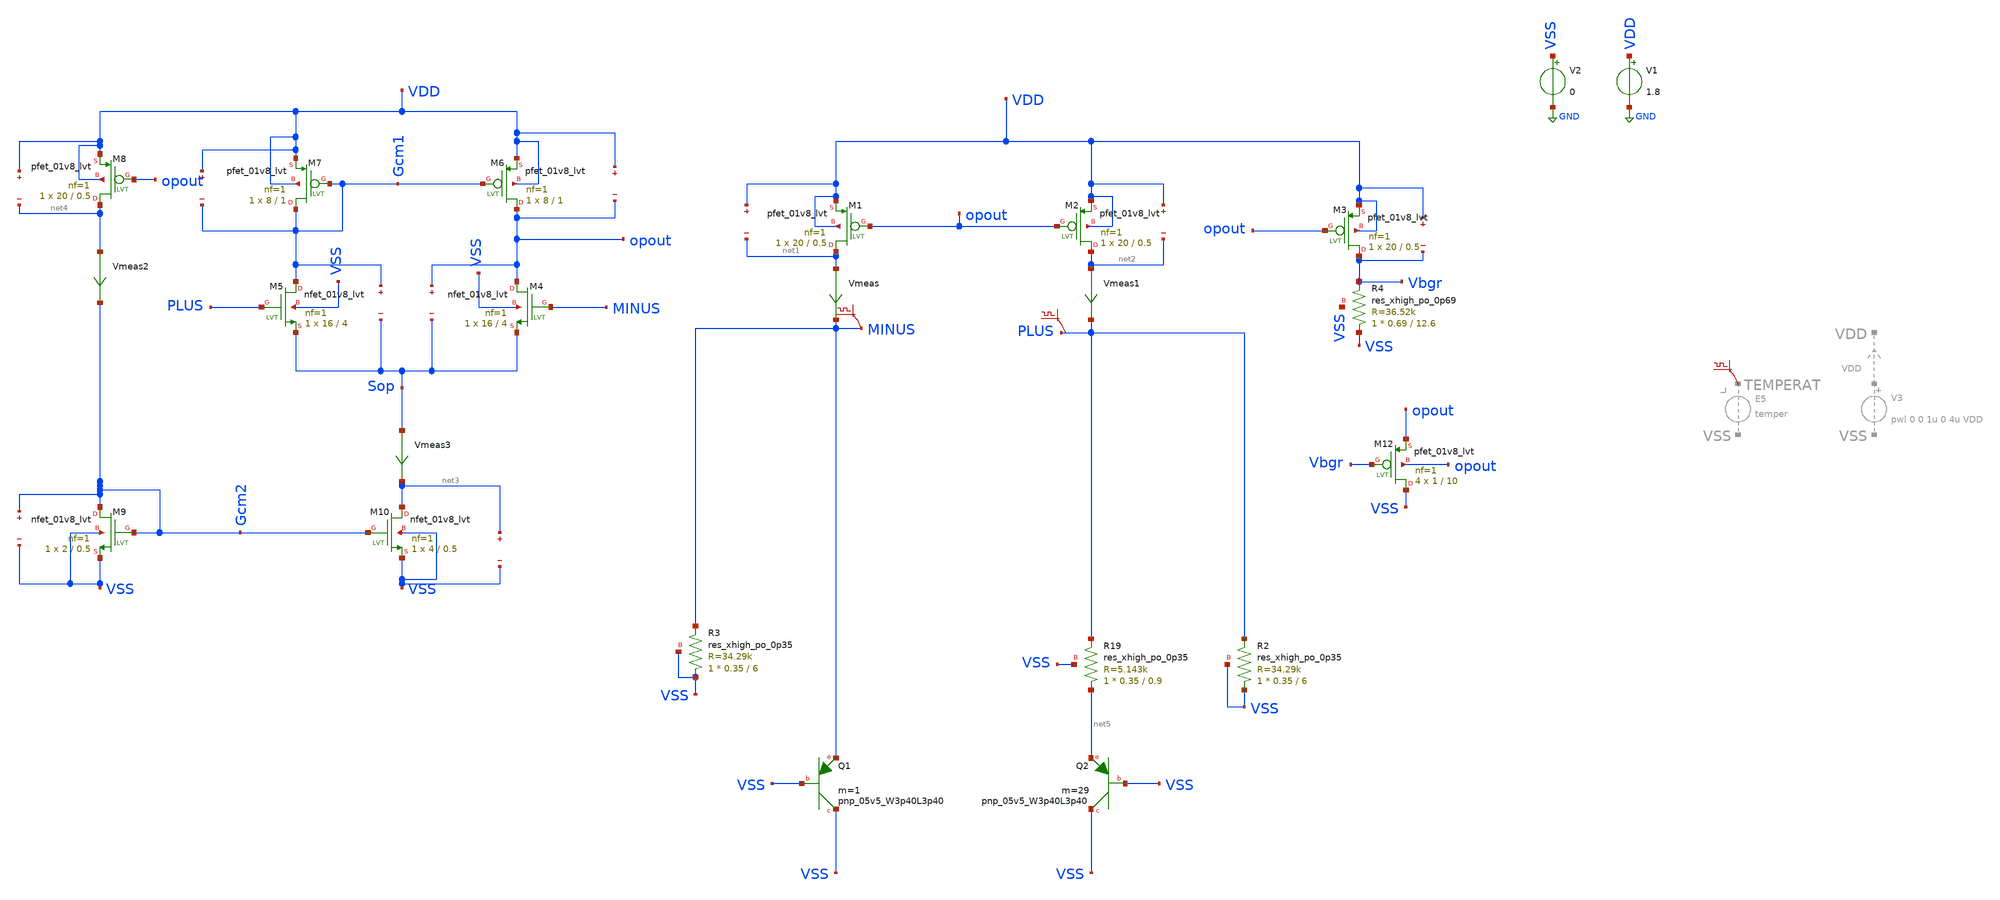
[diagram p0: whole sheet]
** sch_path: xschem/BGRwOpampRes.sch
**.subckt BGRwOpampRes
XQ1 VSS VSS MINUS sky130_fd_pr__pnp_05v5_W3p40L3p40 m=1
XQ2 VSS VSS net5 sky130_fd_pr__pnp_05v5_W3p40L3p40 m=29
XM1 net1 opout VDD VDD sky130_fd_pr__pfet_01v8_lvt L=0.5 W=20 nf=1 ad='int((nf+1)/2) * W/nf * 0.29' as='int((nf+2)/2) * W/nf * 0.29'
+ pd='2*int((nf+1)/2) * (W/nf + 0.29)' ps='2*int((nf+2)/2) * (W/nf + 0.29)' nrd='0.29 / W' nrs='0.29 / W'
+ sa=0 sb=0 sd=0 mult=1 m=1
XM2 net2 opout VDD VDD sky130_fd_pr__pfet_01v8_lvt L=0.5 W=20 nf=1 ad='int((nf+1)/2) * W/nf * 0.29' as='int((nf+2)/2) * W/nf * 0.29'
+ pd='2*int((nf+1)/2) * (W/nf + 0.29)' ps='2*int((nf+2)/2) * (W/nf + 0.29)' nrd='0.29 / W' nrs='0.29 / W'
+ sa=0 sb=0 sd=0 mult=1 m=1
XM3 Vbgr opout VDD VDD sky130_fd_pr__pfet_01v8_lvt L=0.5 W=20 nf=1 ad='int((nf+1)/2) * W/nf * 0.29' as='int((nf+2)/2) * W/nf * 0.29'
+ pd='2*int((nf+1)/2) * (W/nf + 0.29)' ps='2*int((nf+2)/2) * (W/nf + 0.29)' nrd='0.29 / W' nrs='0.29 / W'
+ sa=0 sb=0 sd=0 mult=1 m=1
V1 VDD GND 1.8
V2 VSS GND 0
Vmeas net1 MINUS 0
.save i(vmeas)
Vmeas1 net2 PLUS 0
.save i(vmeas1)
.save v(vdd)
.save v(net1)
.save v(vdd)
.save v(net2)
.save v(vdd)
.save v(vbgr)
XM4 opout MINUS Sop VSS sky130_fd_pr__nfet_01v8_lvt L=4 W=16 nf=1 ad='int((nf+1)/2) * W/nf * 0.29' as='int((nf+2)/2) * W/nf * 0.29'
+ pd='2*int((nf+1)/2) * (W/nf + 0.29)' ps='2*int((nf+2)/2) * (W/nf + 0.29)' nrd='0.29 / W' nrs='0.29 / W'
+ sa=0 sb=0 sd=0 mult=1 m=1
XM5 Gcm1 PLUS Sop VSS sky130_fd_pr__nfet_01v8_lvt L=4 W=16 nf=1 ad='int((nf+1)/2) * W/nf * 0.29' as='int((nf+2)/2) * W/nf * 0.29'
+ pd='2*int((nf+1)/2) * (W/nf + 0.29)' ps='2*int((nf+2)/2) * (W/nf + 0.29)' nrd='0.29 / W' nrs='0.29 / W'
+ sa=0 sb=0 sd=0 mult=1 m=1
XM6 opout Gcm1 VDD VDD sky130_fd_pr__pfet_01v8_lvt L=1 W=8 nf=1 ad='int((nf+1)/2) * W/nf * 0.29' as='int((nf+2)/2) * W/nf * 0.29'
+ pd='2*int((nf+1)/2) * (W/nf + 0.29)' ps='2*int((nf+2)/2) * (W/nf + 0.29)' nrd='0.29 / W' nrs='0.29 / W'
+ sa=0 sb=0 sd=0 mult=1 m=1
.save v(opout)
.save v(sop)
.save v(gcm1)
.save v(sop)
XM10 net3 Gcm2 VSS VSS sky130_fd_pr__nfet_01v8_lvt L=0.5 W=4 nf=1 ad='int((nf+1)/2) * W/nf * 0.29' as='int((nf+2)/2) * W/nf * 0.29'
+ pd='2*int((nf+1)/2) * (W/nf + 0.29)' ps='2*int((nf+2)/2) * (W/nf + 0.29)' nrd='0.29 / W' nrs='0.29 / W'
+ sa=0 sb=0 sd=0 mult=1 m=1
XM9 Gcm2 Gcm2 VSS VSS sky130_fd_pr__nfet_01v8_lvt L=0.5 W=2 nf=1 ad='int((nf+1)/2) * W/nf * 0.29' as='int((nf+2)/2) * W/nf * 0.29'
+ pd='2*int((nf+1)/2) * (W/nf + 0.29)' ps='2*int((nf+2)/2) * (W/nf + 0.29)' nrd='0.29 / W' nrs='0.29 / W'
+ sa=0 sb=0 sd=0 mult=1 m=1
XM7 Gcm1 Gcm1 VDD VDD sky130_fd_pr__pfet_01v8_lvt L=1 W=8 nf=1 ad='int((nf+1)/2) * W/nf * 0.29' as='int((nf+2)/2) * W/nf * 0.29'
+ pd='2*int((nf+1)/2) * (W/nf + 0.29)' ps='2*int((nf+2)/2) * (W/nf + 0.29)' nrd='0.29 / W' nrs='0.29 / W'
+ sa=0 sb=0 sd=0 mult=1 m=1
.save v(vdd)
.save v(gcm1)
.save v(vdd)
.save v(opout)
.save v(net3)
.save v(vss)
.save v(gcm2)
.save v(vss)
Vmeas3 Sop net3 0
.save i(vmeas3)
XM8 net4 opout VDD VDD sky130_fd_pr__pfet_01v8_lvt L=0.5 W=20 nf=1 ad='int((nf+1)/2) * W/nf * 0.29' as='int((nf+2)/2) * W/nf * 0.29'
+ pd='2*int((nf+1)/2) * (W/nf + 0.29)' ps='2*int((nf+2)/2) * (W/nf + 0.29)' nrd='0.29 / W' nrs='0.29 / W'
+ sa=0 sb=0 sd=0 mult=1 m=1
Vmeas2 net4 Gcm2 0
.save i(vmeas2)
.save v(vdd)
.save v(net4)
.save v(minus)
.save v(plus)
XR19 net5 PLUS VSS sky130_fd_pr__res_xhigh_po_0p35 L=0.9 mult=1 m=1
XR3 VSS MINUS VSS sky130_fd_pr__res_xhigh_po_0p35 L=6 mult=1 m=1
XR4 VSS Vbgr VSS sky130_fd_pr__res_xhigh_po_0p69 L=12.6 mult=1 m=1
XM12 VSS Vbgr opout opout sky130_fd_pr__pfet_01v8_lvt L=10 W=1 nf=1 ad='int((nf+1)/2) * W/nf * 0.29'
+ as='int((nf+2)/2) * W/nf * 0.29' pd='2*int((nf+1)/2) * (W/nf + 0.29)' ps='2*int((nf+2)/2) * (W/nf + 0.29)'
+ nrd='0.29 / W' nrs='0.29 / W' sa=0 sb=0 sd=0 mult=4 m=4
XR2 VSS PLUS VSS sky130_fd_pr__res_xhigh_po_0p35 L=6 mult=1 m=1
**** begin user architecture code

** opencircuitdesign pdks install
.lib $::SKYWATER_MODELS/sky130.lib.spice tt


**** end user architecture code
**.ends
.GLOBAL GND
**** begin user architecture code



.options savecurrents
.control


save @m.xm1.msky130_fd_pr__ppet_01v8_lvt[gm]
save @m.xm1.msky130_fd_pr__pfet_01v8_lvt[id]
save @m.xm1.msky130_fd_pr__pfet_01v8_lvt[vgs]
save @m.xm1.msky130_fd_pr__pfet_01v8_lvt[vds]
save @m.xm1.msky130_fd_pr__pfet_01v8_lvt[cgg]
save @m.xm1.msky130_fd_pr__pfet_01v8_lvt[vdsat]
save @m.xm1.msky130_fd_pr__pfet_01v8_lvt[vth]
save @m.xm1.msky130_fd_pr__pfet_01v8_lvt[gds]


save @m.xm2.msky130_fd_pr__pfet_01v8_lvt[gm]
save @m.xm2.msky130_fd_pr__pfet_01v8_lvt[id]
save @m.xm2.msky130_fd_pr__pfet_01v8_lvt[vgs]
save @m.xm2.msky130_fd_pr__pfet_01v8_lvt[vds]
save @m.xm2.msky130_fd_pr__pfet_01v8_lvt[cgg]
save @m.xm2.msky130_fd_pr__pfet_01v8_lvt[vdsat]
save @m.xm2.msky130_fd_pr__pfet_01v8_lvt[vth]
save @m.xm2.msky130_fd_pr__pfet_01v8_lvt[gds]


save @m.xm3.msky130_fd_pr__pfet_01v8_lvt[gm]
save @m.xm3.msky130_fd_pr__pfet_01v8_lvt[id]
save @m.xm3.msky130_fd_pr__pfet_01v8_lvt[vgs]
save @m.xm3.msky130_fd_pr__pfet_01v8_lvt[vds]
save @m.xm3.msky130_fd_pr__pfet_01v8_lvt[cgg]
save @m.xm3.msky130_fd_pr__pfet_01v8_lvt[vdsat]
save @m.xm3.msky130_fd_pr__pfet_01v8_lvt[vth]
save @m.xm3.msky130_fd_pr__pfet_01v8_lvt[gds]



save @q.xq1.qsky130_fd_pr__pnp_05v5_W3p40L3p40[vbe]
save @q.xq2.qsky130_fd_pr__pnp_05v5_W3p40L3p40[vbe]


save @m.xm6.msky130_fd_pr__pfet_01v8_lvt[gm]
save @m.xm6.msky130_fd_pr__pfet_01v8_lvt[id]
save @m.xm6.msky130_fd_pr__pfet_01v8_lvt[vgs]
save @m.xm6.msky130_fd_pr__pfet_01v8_lvt[vds]
save @m.xm6.msky130_fd_pr__pfet_01v8_lvt[cgg]
save @m.xm6.msky130_fd_pr__pfet_01v8_lvt[vdsat]
save @m.xm6.msky130_fd_pr__pfet_01v8_lvt[vth]

save @m.xm7.msky130_fd_pr__pfet_01v8_lvt[gm]
save @m.xm7.msky130_fd_pr__pfet_01v8_lvt[id]
save @m.xm7.msky130_fd_pr__pfet_01v8_lvt[vgs]
save @m.xm7.msky130_fd_pr__pfet_01v8_lvt[vds]
save @m.xm7.msky130_fd_pr__pfet_01v8_lvt[cgg]
save @m.xm7.msky130_fd_pr__pfet_01v8_lvt[vdsat]
save @m.xm7.msky130_fd_pr__pfet_01v8_lvt[vth]



save @m.xm8.msky130_fd_pr__pfet_01v8_lvt[gm]
save @m.xm8.msky130_fd_pr__pfet_01v8_lvt[id]
save @m.xm8.msky130_fd_pr__pfet_01v8_lvt[vgs]
save @m.xm8.msky130_fd_pr__pfet_01v8_lvt[vds]
save @m.xm8.msky130_fd_pr__pfet_01v8_lvt[cgg]
save @m.xm8.msky130_fd_pr__pfet_01v8_lvt[vdsat]
save @m.xm8.msky130_fd_pr__pfet_01v8_lvt[vth]


save @m.xm4.msky130_fd_pr__nfet_01v8_lvt[gm]
save @m.xm4.msky130_fd_pr__nfet_01v8_lvt[id]
save @m.xm4.msky130_fd_pr__nfet_01v8_lvt[vgs]
save @m.xm4.msky130_fd_pr__nfet_01v8_lvt[vds]
save @m.xm4.msky130_fd_pr__nfet_01v8_lvt[cgg]
save @m.xm4.msky130_fd_pr__nfet_01v8_lvt[vdsat]
save @m.xm4.msky130_fd_pr__nfet_01v8_lvt[vth]


save @m.xm5.msky130_fd_pr__nfet_01v8_lvt[gm]
save @m.xm5.msky130_fd_pr__nfet_01v8_lvt[id]
save @m.xm5.msky130_fd_pr__nfet_01v8_lvt[vgs]
save @m.xm5.msky130_fd_pr__nfet_01v8_lvt[vds]
save @m.xm5.msky130_fd_pr__nfet_01v8_lvt[cgg]
save @m.xm5.msky130_fd_pr__nfet_01v8_lvt[vdsat]
save @m.xm5.msky130_fd_pr__nfet_01v8_lvt[vth]



save @m.xm9.msky130_fd_pr__nfet_01v8_lvt[gm]
save @m.xm9.msky130_fd_pr__nfet_01v8_lvt[id]
save @m.xm9.msky130_fd_pr__nfet_01v8_lvt[vgs]
save @m.xm9.msky130_fd_pr__nfet_01v8_lvt[vds]
save @m.xm9.msky130_fd_pr__nfet_01v8_lvt[cgg]
save @m.xm9.msky130_fd_pr__nfet_01v8_lvt[vdsat]
save @m.xm9.msky130_fd_pr__nfet_01v8_lvt[vth]



save @m.xm10.msky130_fd_pr__nfet_01v8_lvt[gm]
save @m.xm10.msky130_fd_pr__nfet_01v8_lvt[id]
save @m.xm10.msky130_fd_pr__nfet_01v8_lvt[vgs]
save @m.xm10.msky130_fd_pr__nfet_01v8_lvt[vds]
save @m.xm10.msky130_fd_pr__nfet_01v8_lvt[cgg]
save @m.xm10.msky130_fd_pr__nfet_01v8_lvt[vdsat]
save @m.xm10.msky130_fd_pr__nfet_01v8_lvt[vth]


save @m.xm11.msky130_fd_pr__nfet_01v8_lvt[gm]
save @m.xm11.msky130_fd_pr__nfet_01v8_lvt[id]
save @m.xm11.msky130_fd_pr__nfet_01v8_lvt[vgs]
save @m.xm11.msky130_fd_pr__nfet_01v8_lvt[vds]
save @m.xm11.msky130_fd_pr__nfet_01v8_lvt[cgg]
save @m.xm11.msky130_fd_pr__nfet_01v8_lvt[vdsat]
save @m.xm11.msky130_fd_pr__nfet_01v8_lvt[vth]
save all
op
write BGRwOpampRes.raw
dc TEMP -40 140 1
plot deriv(Vbgr)
plot Vbgr

.endc



**** end user architecture code
.end
